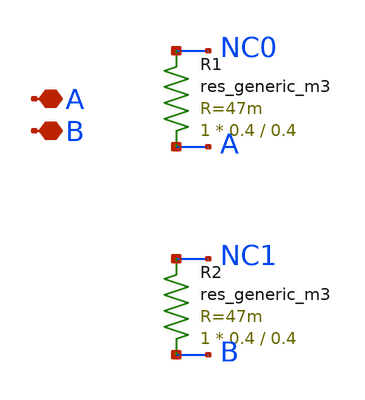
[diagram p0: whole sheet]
** sch_path: ip/sun_pll_sky130nm/design/SUN_PLL_SKY130NM/CAP_LPF.sch
**.subckt CAP_LPF A B
*.iopin A
*.iopin B
R1 A NC0 sky130_fd_pr__res_generic_m3 W=0.4 L=0.4 m=1
R2 B NC1 sky130_fd_pr__res_generic_m3 W=0.4 L=0.4 m=1
**.ends
.end
